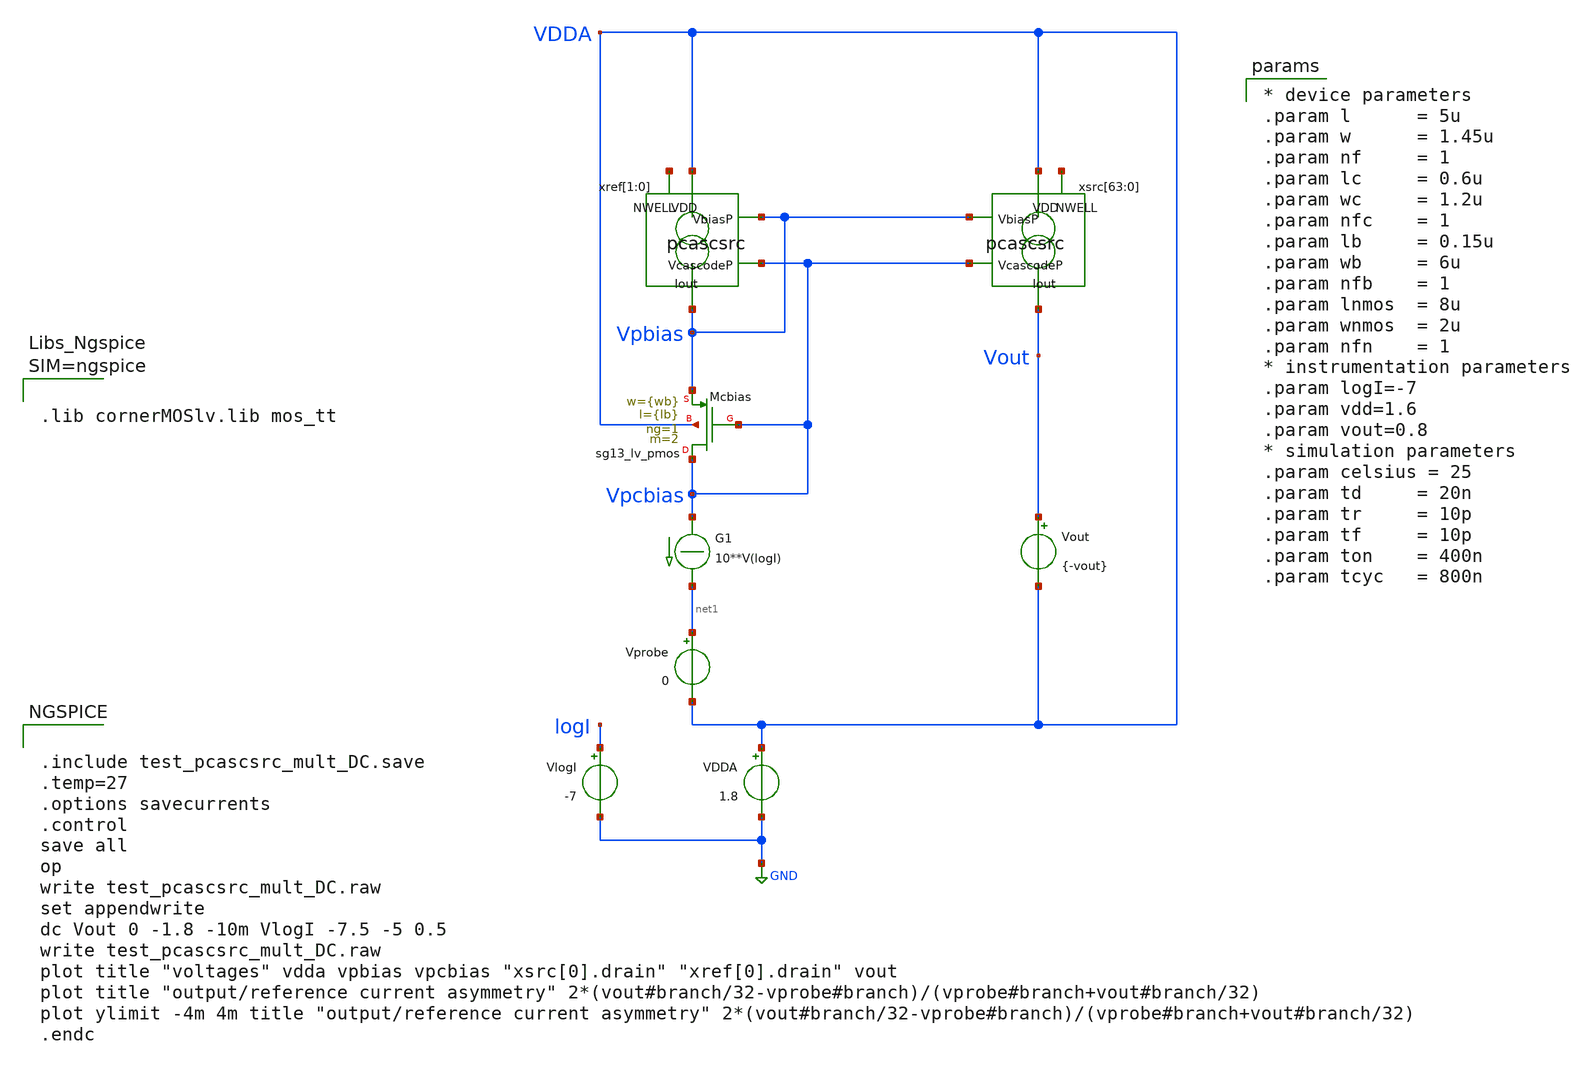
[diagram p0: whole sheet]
** sch_path: xschem/test_pcascsrc_mult_DC.sch
**.subckt test_pcascsrc_mult_DC
Vout Vout VDDA {-vout}
.save i(vout)
Vprobe net1 VDDA 0
.save i(vprobe)
G1 Vpcbias net1 CUR=' 10**V(logI) '
VlogI logI GND -7
.save i(vlogi)
xref[1] VDDA Vpbias Vpcbias Vpbias net2[1] pcascsrc
xref[0] VDDA Vpbias Vpcbias Vpbias net2[0] pcascsrc
xsrc[63] VDDA Vpbias Vpcbias Vout net3[63] pcascsrc
xsrc[62] VDDA Vpbias Vpcbias Vout net3[62] pcascsrc
xsrc[61] VDDA Vpbias Vpcbias Vout net3[61] pcascsrc
xsrc[60] VDDA Vpbias Vpcbias Vout net3[60] pcascsrc
xsrc[59] VDDA Vpbias Vpcbias Vout net3[59] pcascsrc
xsrc[58] VDDA Vpbias Vpcbias Vout net3[58] pcascsrc
xsrc[57] VDDA Vpbias Vpcbias Vout net3[57] pcascsrc
xsrc[56] VDDA Vpbias Vpcbias Vout net3[56] pcascsrc
xsrc[55] VDDA Vpbias Vpcbias Vout net3[55] pcascsrc
xsrc[54] VDDA Vpbias Vpcbias Vout net3[54] pcascsrc
xsrc[53] VDDA Vpbias Vpcbias Vout net3[53] pcascsrc
xsrc[52] VDDA Vpbias Vpcbias Vout net3[52] pcascsrc
xsrc[51] VDDA Vpbias Vpcbias Vout net3[51] pcascsrc
xsrc[50] VDDA Vpbias Vpcbias Vout net3[50] pcascsrc
xsrc[49] VDDA Vpbias Vpcbias Vout net3[49] pcascsrc
xsrc[48] VDDA Vpbias Vpcbias Vout net3[48] pcascsrc
xsrc[47] VDDA Vpbias Vpcbias Vout net3[47] pcascsrc
xsrc[46] VDDA Vpbias Vpcbias Vout net3[46] pcascsrc
xsrc[45] VDDA Vpbias Vpcbias Vout net3[45] pcascsrc
xsrc[44] VDDA Vpbias Vpcbias Vout net3[44] pcascsrc
xsrc[43] VDDA Vpbias Vpcbias Vout net3[43] pcascsrc
xsrc[42] VDDA Vpbias Vpcbias Vout net3[42] pcascsrc
xsrc[41] VDDA Vpbias Vpcbias Vout net3[41] pcascsrc
xsrc[40] VDDA Vpbias Vpcbias Vout net3[40] pcascsrc
xsrc[39] VDDA Vpbias Vpcbias Vout net3[39] pcascsrc
xsrc[38] VDDA Vpbias Vpcbias Vout net3[38] pcascsrc
xsrc[37] VDDA Vpbias Vpcbias Vout net3[37] pcascsrc
xsrc[36] VDDA Vpbias Vpcbias Vout net3[36] pcascsrc
xsrc[35] VDDA Vpbias Vpcbias Vout net3[35] pcascsrc
xsrc[34] VDDA Vpbias Vpcbias Vout net3[34] pcascsrc
xsrc[33] VDDA Vpbias Vpcbias Vout net3[33] pcascsrc
xsrc[32] VDDA Vpbias Vpcbias Vout net3[32] pcascsrc
xsrc[31] VDDA Vpbias Vpcbias Vout net3[31] pcascsrc
xsrc[30] VDDA Vpbias Vpcbias Vout net3[30] pcascsrc
xsrc[29] VDDA Vpbias Vpcbias Vout net3[29] pcascsrc
xsrc[28] VDDA Vpbias Vpcbias Vout net3[28] pcascsrc
xsrc[27] VDDA Vpbias Vpcbias Vout net3[27] pcascsrc
xsrc[26] VDDA Vpbias Vpcbias Vout net3[26] pcascsrc
xsrc[25] VDDA Vpbias Vpcbias Vout net3[25] pcascsrc
xsrc[24] VDDA Vpbias Vpcbias Vout net3[24] pcascsrc
xsrc[23] VDDA Vpbias Vpcbias Vout net3[23] pcascsrc
xsrc[22] VDDA Vpbias Vpcbias Vout net3[22] pcascsrc
xsrc[21] VDDA Vpbias Vpcbias Vout net3[21] pcascsrc
xsrc[20] VDDA Vpbias Vpcbias Vout net3[20] pcascsrc
xsrc[19] VDDA Vpbias Vpcbias Vout net3[19] pcascsrc
xsrc[18] VDDA Vpbias Vpcbias Vout net3[18] pcascsrc
xsrc[17] VDDA Vpbias Vpcbias Vout net3[17] pcascsrc
xsrc[16] VDDA Vpbias Vpcbias Vout net3[16] pcascsrc
xsrc[15] VDDA Vpbias Vpcbias Vout net3[15] pcascsrc
xsrc[14] VDDA Vpbias Vpcbias Vout net3[14] pcascsrc
xsrc[13] VDDA Vpbias Vpcbias Vout net3[13] pcascsrc
xsrc[12] VDDA Vpbias Vpcbias Vout net3[12] pcascsrc
xsrc[11] VDDA Vpbias Vpcbias Vout net3[11] pcascsrc
xsrc[10] VDDA Vpbias Vpcbias Vout net3[10] pcascsrc
xsrc[9] VDDA Vpbias Vpcbias Vout net3[9] pcascsrc
xsrc[8] VDDA Vpbias Vpcbias Vout net3[8] pcascsrc
xsrc[7] VDDA Vpbias Vpcbias Vout net3[7] pcascsrc
xsrc[6] VDDA Vpbias Vpcbias Vout net3[6] pcascsrc
xsrc[5] VDDA Vpbias Vpcbias Vout net3[5] pcascsrc
xsrc[4] VDDA Vpbias Vpcbias Vout net3[4] pcascsrc
xsrc[3] VDDA Vpbias Vpcbias Vout net3[3] pcascsrc
xsrc[2] VDDA Vpbias Vpcbias Vout net3[2] pcascsrc
xsrc[1] VDDA Vpbias Vpcbias Vout net3[1] pcascsrc
xsrc[0] VDDA Vpbias Vpcbias Vout net3[0] pcascsrc
VDDA VDDA GND 1.8
.save i(vdda)
XMcbias Vpcbias Vpcbias Vpbias VDDA sg13_lv_pmos w={wb} l={lb} ng=1 m=2 mm_ok=1
**** begin user architecture code


.include test_pcascsrc_mult_DC.save
.temp=27
.options savecurrents
.control
save all
op
write test_pcascsrc_mult_DC.raw
set appendwrite
dc Vout 0 -1.8 -10m VlogI -7.5 -5 0.5
write test_pcascsrc_mult_DC.raw
plot title "voltages" vdda vpbias vpcbias "xsrc[0].drain" "xref[0].drain" vout
plot title "output/reference current asymmetry"
+ 2*(vout#branch/32-vprobe#branch)/(vprobe#branch+vout#branch/32)
plot ylimit -4m 4m title "output/reference current asymmetry"
+ 2*(vout#branch/32-vprobe#branch)/(vprobe#branch+vout#branch/32)
.endc





.lib cornerMOSlv.lib mos_tt




* device parameters
.param l      = 5u
.param w      = 1.45u
.param nf     = 1
.param lc     = 0.6u
.param wc     = 1.2u
.param nfc    = 1
.param lb     = 0.15u
.param wb     = 6u
.param nfb    = 1
.param lnmos  = 8u
.param wnmos  = 2u
.param nfn    = 1
* instrumentation parameters
.param logI=-7
.param vdd=1.6
.param vout=0.8
* simulation parameters
.param celsius = 25
.param td     = 20n
.param tr     = 10p
.param tf     = 10p
.param ton    = 400n
.param tcyc   = 800n


**** end user architecture code
**.ends

* expanding   symbol:  pcascsrc.sym # of pins=5
** sym_path: xschem/pcascsrc.sym
** sch_path: xschem/pcascsrc.sch
.subckt pcascsrc VDD VbiasP VcascodeP Iout NWELL
*.ipin VcascodeP
*.ipin VbiasP
*.opin Iout
*.ipin VDD
*.iopin NWELL
XMsrc drain VbiasP VDD NWELL sg13_lv_pmos w=0.74u l=2u ng=1 m=1 mm_ok=1
XMcasc Iout VcascodeP drain NWELL sg13_lv_pmos w=0.3u l=0.3u ng=1 m=1 mm_ok=1
.ends

.GLOBAL GND
.end
